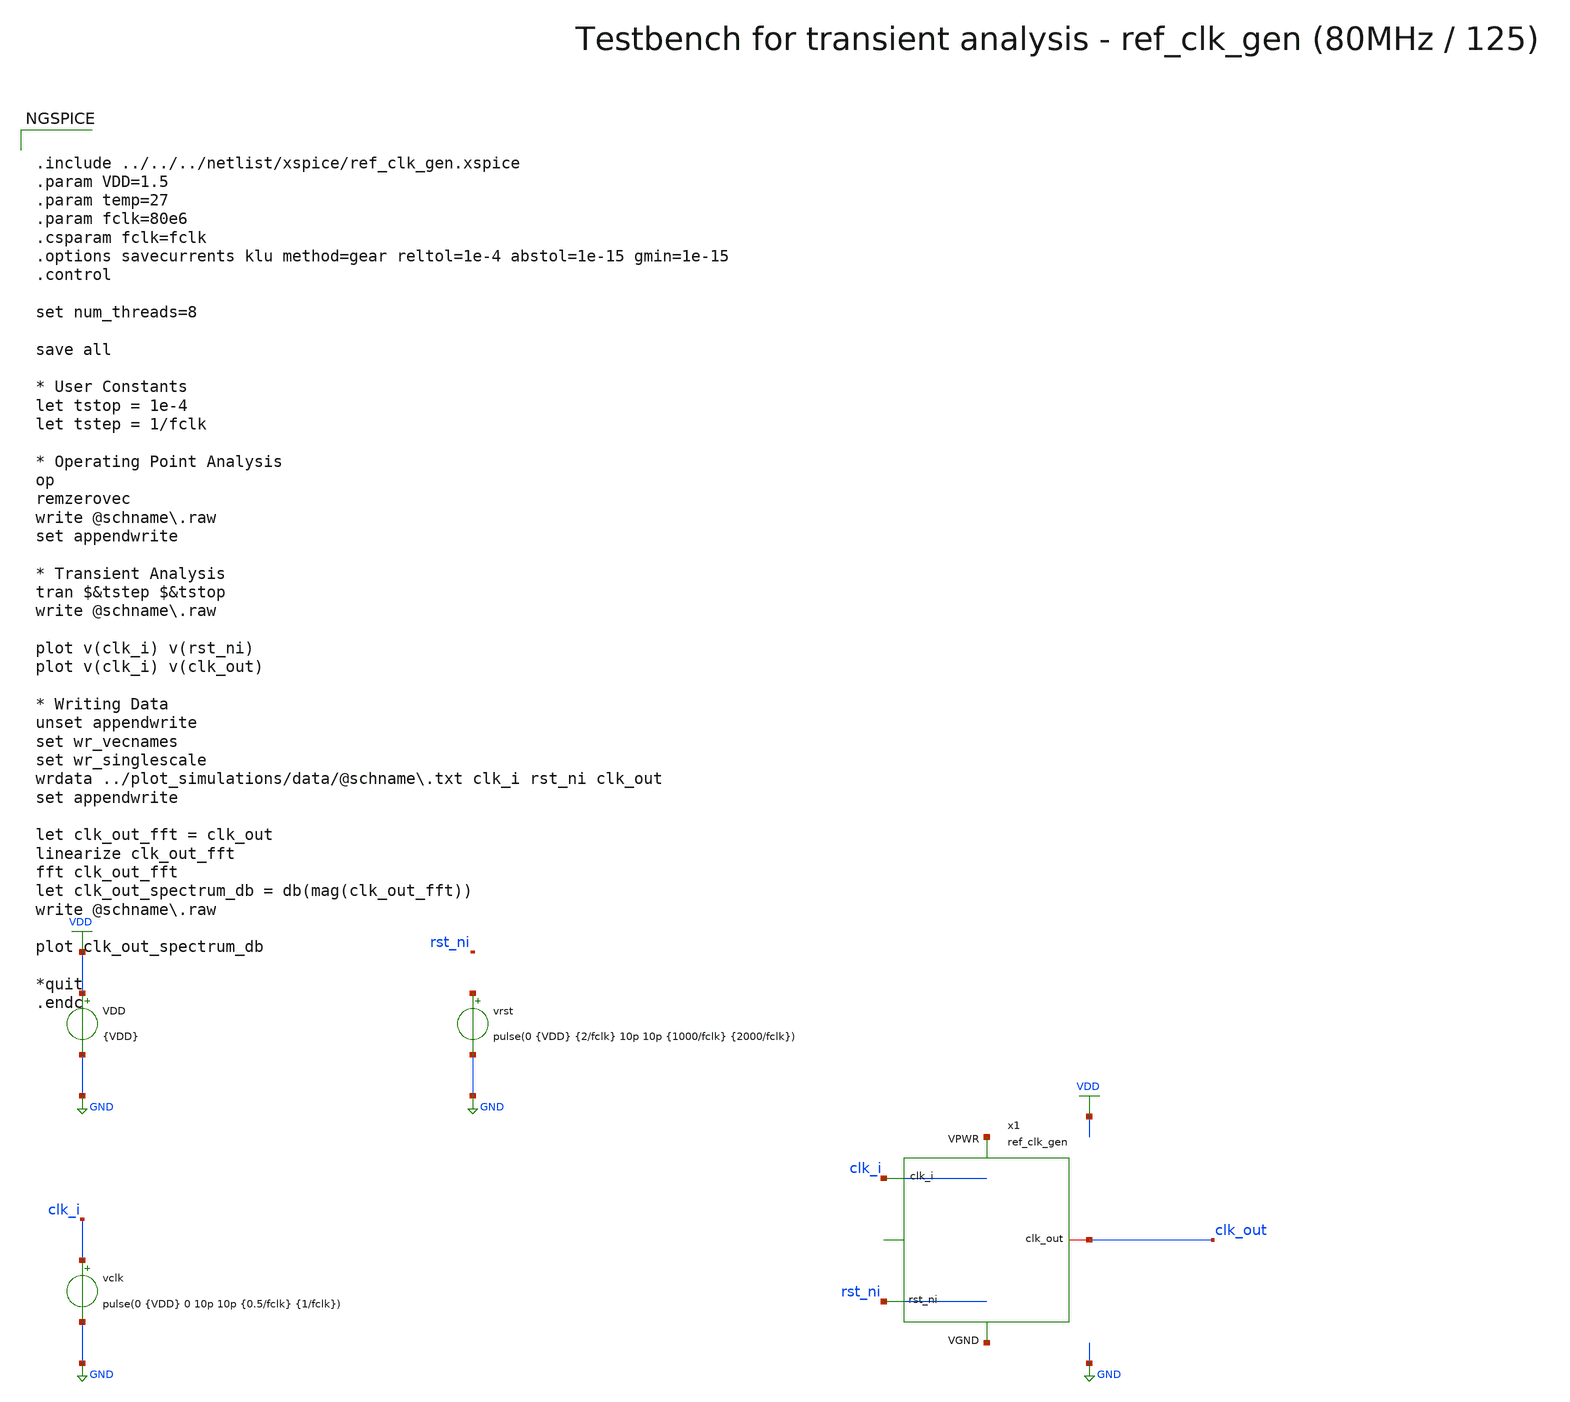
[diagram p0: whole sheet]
** sch_path: macros/heichips26_ook/macros/ref_clk_gen/testbenches/xschem/ref_clk_gen_tb_tran.sch
**.subckt ref_clk_gen_tb_tran
VDD VDD GND {VDD}
vclk clk_i GND pulse(0 {VDD} 0 10p 10p {0.5/fclk} {1/fclk})
vrst net1 GND pulse(0 {VDD} {2/fclk} 10p 10p {1000/fclk} {2000/fclk})
x1 net2 net3 clk_i rst_ni clk_out ref_clk_gen
**** begin user architecture code


.include ../../../netlist/xspice/ref_clk_gen.xspice
.param VDD=1.5
.param temp=27
.param fclk=80e6
.csparam fclk=fclk
.options savecurrents klu method=gear reltol=1e-4 abstol=1e-15 gmin=1e-15
.control

set num_threads=8

save all

* User Constants
let tstop = 1e-4
let tstep = 1/fclk

* Operating Point Analysis
op
remzerovec
write @schname\.raw
set appendwrite

* Transient Analysis
tran $&tstep $&tstop
write @schname\.raw

plot v(clk_i) v(rst_ni)
plot v(clk_i) v(clk_out)

* Writing Data
unset appendwrite
set wr_vecnames
set wr_singlescale
wrdata ../plot_simulations/data/@schname\.txt clk_i rst_ni clk_out
set appendwrite

let clk_out_fft = clk_out
linearize clk_out_fft
fft clk_out_fft
let clk_out_spectrum_db = db(mag(clk_out_fft))
write @schname\.raw

plot clk_out_spectrum_db

*quit
.endc


.lib cornerMOSlv.lib mos_tt
.lib cornerMOShv.lib mos_tt
.lib cornerRES.lib res_typ
.lib cornerDIO.lib dio_tt

**** end user architecture code
**.ends
.GLOBAL GND
.GLOBAL VDD
.end
